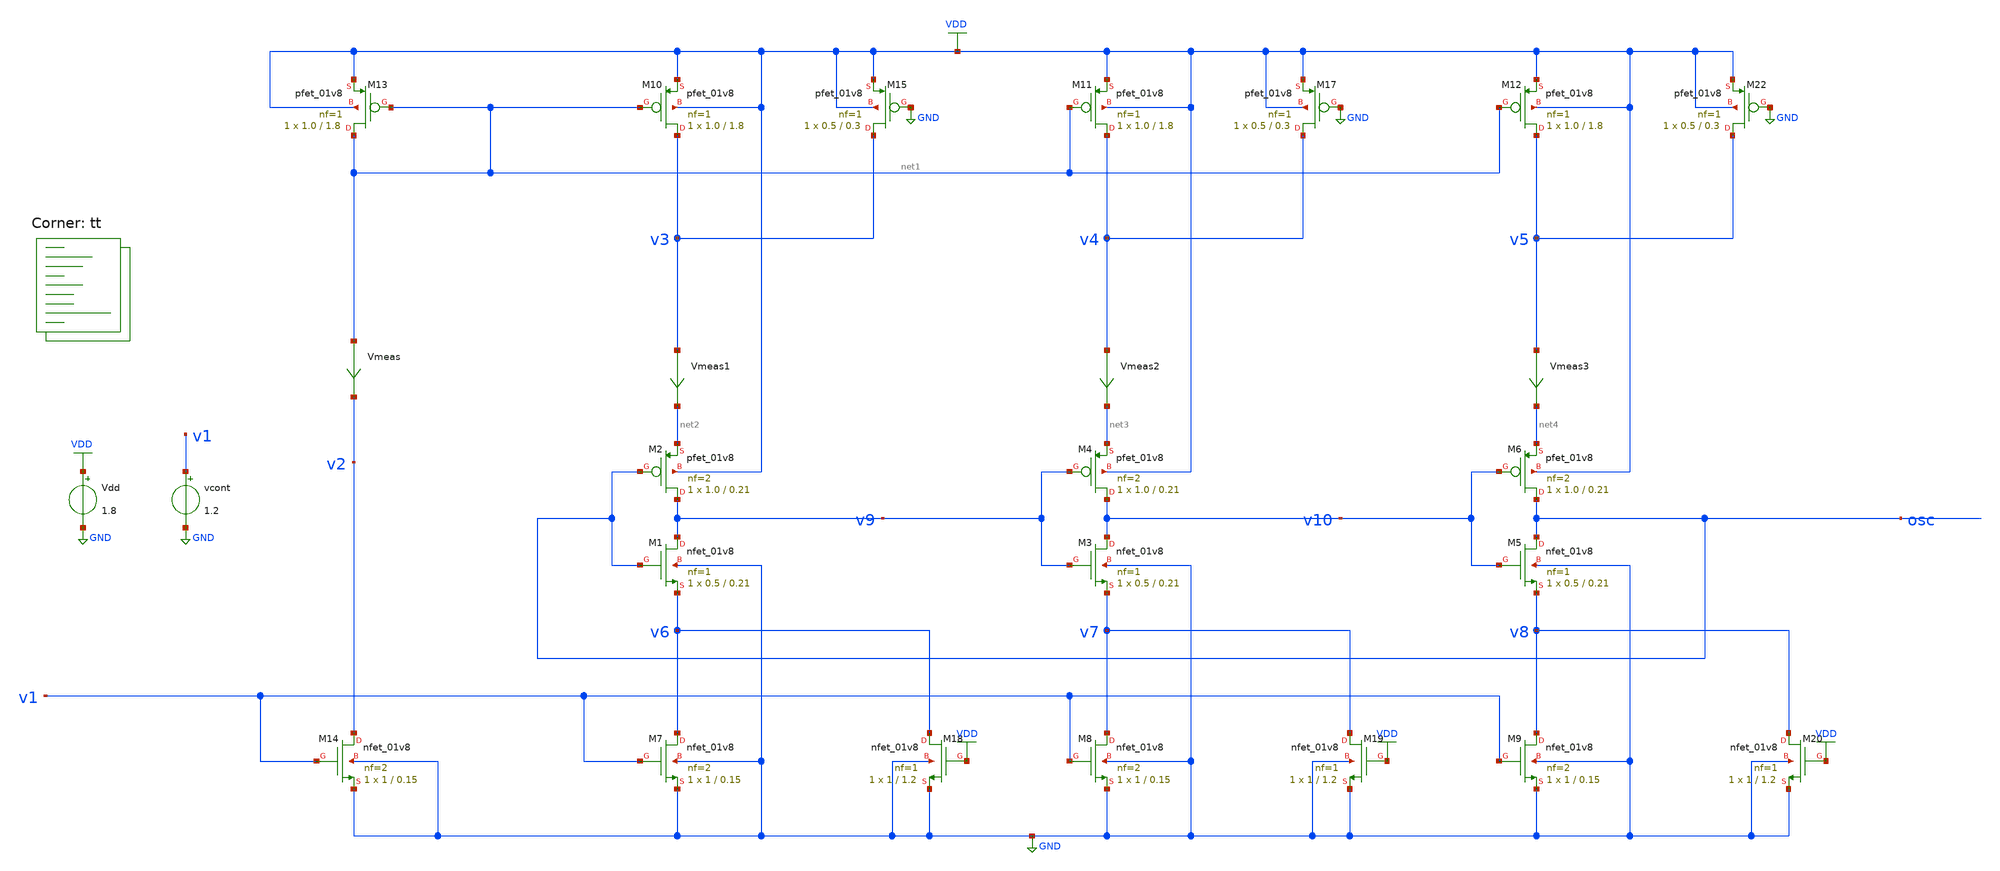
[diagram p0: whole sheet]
** sch_path: projects/pll/vco/xschem_ngspice/tb_current_starved_VCO9.sch
**.subckt tb_current_starved_VCO9
XM1 v9 osc v6 GND sky130_fd_pr__nfet_01v8 L=0.21 W=0.5 nf=1 ad='int((nf+1)/2) * W/nf * 0.29' as='int((nf+2)/2) * W/nf * 0.29'
+ pd='2*int((nf+1)/2) * (W/nf + 0.29)' ps='2*int((nf+2)/2) * (W/nf + 0.29)' nrd='0.29 / W' nrs='0.29 / W'
+ sa=0 sb=0 sd=0 mult=1 m=1
XM2 v9 osc net2 VDD sky130_fd_pr__pfet_01v8 L=0.21 W=1.0 nf=2 ad='int((nf+1)/2) * W/nf * 0.29' as='int((nf+2)/2) * W/nf * 0.29'
+ pd='2*int((nf+1)/2) * (W/nf + 0.29)' ps='2*int((nf+2)/2) * (W/nf + 0.29)' nrd='0.29 / W' nrs='0.29 / W'
+ sa=0 sb=0 sd=0 mult=1 m=1
XM3 v10 v9 v7 GND sky130_fd_pr__nfet_01v8 L=0.21 W=0.5 nf=1 ad='int((nf+1)/2) * W/nf * 0.29' as='int((nf+2)/2) * W/nf * 0.29'
+ pd='2*int((nf+1)/2) * (W/nf + 0.29)' ps='2*int((nf+2)/2) * (W/nf + 0.29)' nrd='0.29 / W' nrs='0.29 / W'
+ sa=0 sb=0 sd=0 mult=1 m=1
XM4 v10 v9 net3 VDD sky130_fd_pr__pfet_01v8 L=0.21 W=1.0 nf=2 ad='int((nf+1)/2) * W/nf * 0.29' as='int((nf+2)/2) * W/nf * 0.29'
+ pd='2*int((nf+1)/2) * (W/nf + 0.29)' ps='2*int((nf+2)/2) * (W/nf + 0.29)' nrd='0.29 / W' nrs='0.29 / W'
+ sa=0 sb=0 sd=0 mult=1 m=1
XM5 osc v10 v8 GND sky130_fd_pr__nfet_01v8 L=0.21 W=0.5 nf=1 ad='int((nf+1)/2) * W/nf * 0.29' as='int((nf+2)/2) * W/nf * 0.29'
+ pd='2*int((nf+1)/2) * (W/nf + 0.29)' ps='2*int((nf+2)/2) * (W/nf + 0.29)' nrd='0.29 / W' nrs='0.29 / W'
+ sa=0 sb=0 sd=0 mult=1 m=1
XM6 osc v10 net4 VDD sky130_fd_pr__pfet_01v8 L=0.21 W=1.0 nf=2 ad='int((nf+1)/2) * W/nf * 0.29' as='int((nf+2)/2) * W/nf * 0.29'
+ pd='2*int((nf+1)/2) * (W/nf + 0.29)' ps='2*int((nf+2)/2) * (W/nf + 0.29)' nrd='0.29 / W' nrs='0.29 / W'
+ sa=0 sb=0 sd=0 mult=1 m=1
XM7 v6 v1 GND GND sky130_fd_pr__nfet_01v8 L=0.15 W=1 nf=2 ad='int((nf+1)/2) * W/nf * 0.29' as='int((nf+2)/2) * W/nf * 0.29'
+ pd='2*int((nf+1)/2) * (W/nf + 0.29)' ps='2*int((nf+2)/2) * (W/nf + 0.29)' nrd='0.29 / W' nrs='0.29 / W'
+ sa=0 sb=0 sd=0 mult=1 m=1
XM8 v7 v1 GND GND sky130_fd_pr__nfet_01v8 L=0.15 W=1 nf=2 ad='int((nf+1)/2) * W/nf * 0.29' as='int((nf+2)/2) * W/nf * 0.29'
+ pd='2*int((nf+1)/2) * (W/nf + 0.29)' ps='2*int((nf+2)/2) * (W/nf + 0.29)' nrd='0.29 / W' nrs='0.29 / W'
+ sa=0 sb=0 sd=0 mult=1 m=1
XM9 v8 v1 GND GND sky130_fd_pr__nfet_01v8 L=0.15 W=1 nf=2 ad='int((nf+1)/2) * W/nf * 0.29' as='int((nf+2)/2) * W/nf * 0.29'
+ pd='2*int((nf+1)/2) * (W/nf + 0.29)' ps='2*int((nf+2)/2) * (W/nf + 0.29)' nrd='0.29 / W' nrs='0.29 / W'
+ sa=0 sb=0 sd=0 mult=1 m=1
XM10 v3 net1 VDD VDD sky130_fd_pr__pfet_01v8 L=1.8 W=1.0 nf=1 ad='int((nf+1)/2) * W/nf * 0.29' as='int((nf+2)/2) * W/nf * 0.29'
+ pd='2*int((nf+1)/2) * (W/nf + 0.29)' ps='2*int((nf+2)/2) * (W/nf + 0.29)' nrd='0.29 / W' nrs='0.29 / W'
+ sa=0 sb=0 sd=0 mult=1 m=1
XM11 v4 net1 VDD VDD sky130_fd_pr__pfet_01v8 L=1.8 W=1.0 nf=1 ad='int((nf+1)/2) * W/nf * 0.29' as='int((nf+2)/2) * W/nf * 0.29'
+ pd='2*int((nf+1)/2) * (W/nf + 0.29)' ps='2*int((nf+2)/2) * (W/nf + 0.29)' nrd='0.29 / W' nrs='0.29 / W'
+ sa=0 sb=0 sd=0 mult=1 m=1
XM12 v5 net1 VDD VDD sky130_fd_pr__pfet_01v8 L=1.8 W=1.0 nf=1 ad='int((nf+1)/2) * W/nf * 0.29' as='int((nf+2)/2) * W/nf * 0.29'
+ pd='2*int((nf+1)/2) * (W/nf + 0.29)' ps='2*int((nf+2)/2) * (W/nf + 0.29)' nrd='0.29 / W' nrs='0.29 / W'
+ sa=0 sb=0 sd=0 mult=1 m=1
Vdd VDD GND 1.8
vcont v1 GND 1.2
XM18 v6 VDD GND GND sky130_fd_pr__nfet_01v8 L=1.2 W=1 nf=1 ad='int((nf+1)/2) * W/nf * 0.29' as='int((nf+2)/2) * W/nf * 0.29'
+ pd='2*int((nf+1)/2) * (W/nf + 0.29)' ps='2*int((nf+2)/2) * (W/nf + 0.29)' nrd='0.29 / W' nrs='0.29 / W'
+ sa=0 sb=0 sd=0 mult=1 m=1
XM19 v7 VDD GND GND sky130_fd_pr__nfet_01v8 L=1.2 W=1 nf=1 ad='int((nf+1)/2) * W/nf * 0.29' as='int((nf+2)/2) * W/nf * 0.29'
+ pd='2*int((nf+1)/2) * (W/nf + 0.29)' ps='2*int((nf+2)/2) * (W/nf + 0.29)' nrd='0.29 / W' nrs='0.29 / W'
+ sa=0 sb=0 sd=0 mult=1 m=1
XM20 v8 VDD GND GND sky130_fd_pr__nfet_01v8 L=1.2 W=1 nf=1 ad='int((nf+1)/2) * W/nf * 0.29' as='int((nf+2)/2) * W/nf * 0.29'
+ pd='2*int((nf+1)/2) * (W/nf + 0.29)' ps='2*int((nf+2)/2) * (W/nf + 0.29)' nrd='0.29 / W' nrs='0.29 / W'
+ sa=0 sb=0 sd=0 mult=1 m=1
XM15 v3 GND VDD VDD sky130_fd_pr__pfet_01v8 L=0.3 W=0.5 nf=1 ad='int((nf+1)/2) * W/nf * 0.29' as='int((nf+2)/2) * W/nf * 0.29'
+ pd='2*int((nf+1)/2) * (W/nf + 0.29)' ps='2*int((nf+2)/2) * (W/nf + 0.29)' nrd='0.29 / W' nrs='0.29 / W'
+ sa=0 sb=0 sd=0 mult=1 m=1
XM17 v4 GND VDD VDD sky130_fd_pr__pfet_01v8 L=0.3 W=0.5 nf=1 ad='int((nf+1)/2) * W/nf * 0.29' as='int((nf+2)/2) * W/nf * 0.29'
+ pd='2*int((nf+1)/2) * (W/nf + 0.29)' ps='2*int((nf+2)/2) * (W/nf + 0.29)' nrd='0.29 / W' nrs='0.29 / W'
+ sa=0 sb=0 sd=0 mult=1 m=1
XM22 v5 GND VDD VDD sky130_fd_pr__pfet_01v8 L=0.3 W=0.5 nf=1 ad='int((nf+1)/2) * W/nf * 0.29' as='int((nf+2)/2) * W/nf * 0.29'
+ pd='2*int((nf+1)/2) * (W/nf + 0.29)' ps='2*int((nf+2)/2) * (W/nf + 0.29)' nrd='0.29 / W' nrs='0.29 / W'
+ sa=0 sb=0 sd=0 mult=1 m=1
XM13 net1 net1 VDD VDD sky130_fd_pr__pfet_01v8 L=1.8 W=1.0 nf=1 ad='int((nf+1)/2) * W/nf * 0.29' as='int((nf+2)/2) * W/nf * 0.29'
+ pd='2*int((nf+1)/2) * (W/nf + 0.29)' ps='2*int((nf+2)/2) * (W/nf + 0.29)' nrd='0.29 / W' nrs='0.29 / W'
+ sa=0 sb=0 sd=0 mult=1 m=1
XM14 v2 v1 GND GND sky130_fd_pr__nfet_01v8 L=0.15 W=1 nf=2 ad='int((nf+1)/2) * W/nf * 0.29' as='int((nf+2)/2) * W/nf * 0.29'
+ pd='2*int((nf+1)/2) * (W/nf + 0.29)' ps='2*int((nf+2)/2) * (W/nf + 0.29)' nrd='0.29 / W' nrs='0.29 / W'
+ sa=0 sb=0 sd=0 mult=1 m=1
Vmeas net1 v2 0
.save i(vmeas)
Vmeas1 v3 net2 0
.save i(vmeas1)
Vmeas2 v4 net3 0
.save i(vmeas2)
Vmeas3 v5 net4 0
.save i(vmeas3)
**** begin user architecture code
.lib $::SKYWATER_MODELS/sky130.lib.spice tt



.option method=gear
.option wnflag=1


*.ic v(vcont)=1.2

*.temp = 75

* Xmeasure osc freq2 measure_Kvco thresh=0.9 dir=1

.control

  * pre_osdi ./measure_Kvco.osdi

  let v_cont_start = 0.0
  let v_cont_stop = 1.9

  dowhile v_cont_start <= v_cont_stop
    alter vcont $&v_cont_start
    save v(vcont) v(osc) v(v1) v(v2) v(v3) v(v4) v(v5) v(v6) v(v7) v(v8) v(v9) v(v10) i(vmeas)
+ i(vmeas1) i(vmeas2) i(vmeas3)
    * save all
    tran 1ps 30ns
    remzerovec
    write tb_current_starved_VCO9_{$&v_cont_start}.raw
    * write tb_current_starved_VCO9.raw
    linearize v(vcont) v(osc) v(v1) v(v2) v(v3) v(v4) v(v5) v(v6) v(v7) v(v8) v(v9) v(v10) i(vmeas)
+ i(vmeas1) i(vmeas2) i(vmeas3)
    let filename = v_cont_start * 100
    wrdata /foss/designs/my_design/projects/pll/vco/xschem_ngspice/tb_current_starved_VCO9_{$&filename}.txt
+ v(osc)
    set appendwrite

    reset
    let v_cont_start = v_cont_start + 0.1
  end
.endc




**** end user architecture code
**.ends
.GLOBAL VDD
.GLOBAL GND
.end
